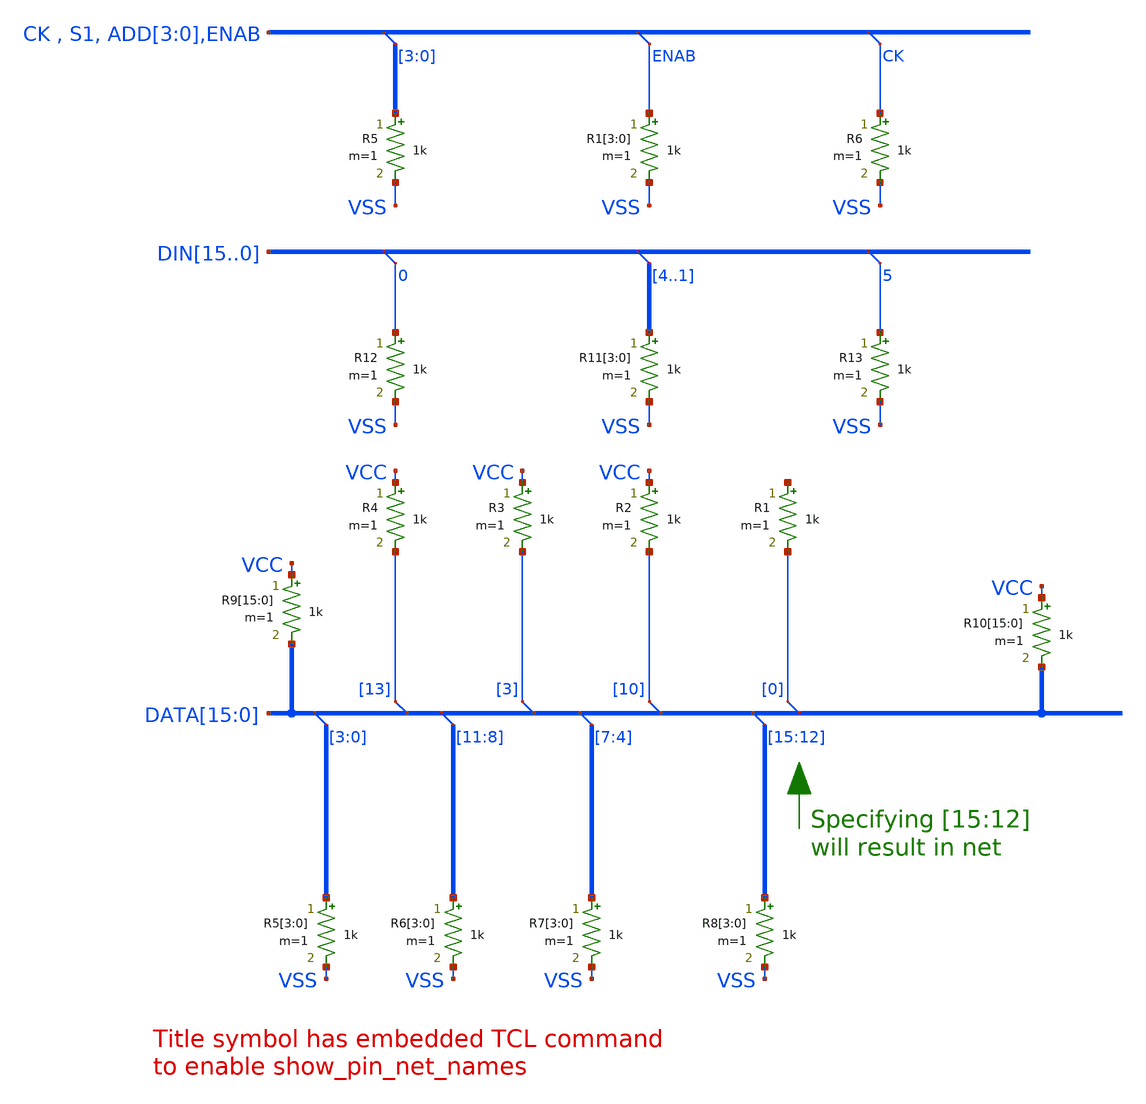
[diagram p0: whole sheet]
** sch_path: xschem_library/examples/test_bus_tap.sch
**.subckt test_bus_tap
* tap: DATA[15:0] --> DATA[3]
* tap: DATA[15:0] --> DATA[13]
* tap: DATA[15:0] --> DATA[7:4]
* tap: DATA[15:0] --> DATA[11:8]
* tap: DATA[15:0] --> DATA[3:0]
* tap: DATA[15:0] --> DATA[10]
* tap: DATA[15:0] --> DATA[0]
R1 net1 DATA[0] 1k m=1
R2 VCC DATA[10] 1k m=1
R3 VCC DATA[3] 1k m=1
R4 VCC DATA[13] 1k m=1
R5[3] DATA[3] VSS 1k m=1
R5[2] DATA[2] VSS 1k m=1
R5[1] DATA[1] VSS 1k m=1
R5[0] DATA[0] VSS 1k m=1
R6[3] DATA[11] VSS 1k m=1
R6[2] DATA[10] VSS 1k m=1
R6[1] DATA[9] VSS 1k m=1
R6[0] DATA[8] VSS 1k m=1
R7[3] DATA[7] VSS 1k m=1
R7[2] DATA[6] VSS 1k m=1
R7[1] DATA[5] VSS 1k m=1
R7[0] DATA[4] VSS 1k m=1
R8[3] DATA[15] VSS 1k m=1
R8[2] DATA[14] VSS 1k m=1
R8[1] DATA[13] VSS 1k m=1
R8[0] DATA[12] VSS 1k m=1
* tap: DATA[15:0] --> DATA[15:12]
R9[15] VCC DATA[15] 1k m=1
R9[14] VCC DATA[14] 1k m=1
R9[13] VCC DATA[13] 1k m=1
R9[12] VCC DATA[12] 1k m=1
R9[11] VCC DATA[11] 1k m=1
R9[10] VCC DATA[10] 1k m=1
R9[9] VCC DATA[9] 1k m=1
R9[8] VCC DATA[8] 1k m=1
R9[7] VCC DATA[7] 1k m=1
R9[6] VCC DATA[6] 1k m=1
R9[5] VCC DATA[5] 1k m=1
R9[4] VCC DATA[4] 1k m=1
R9[3] VCC DATA[3] 1k m=1
R9[2] VCC DATA[2] 1k m=1
R9[1] VCC DATA[1] 1k m=1
R9[0] VCC DATA[0] 1k m=1
R10[15] VCC DATA[15] 1k m=1
R10[14] VCC DATA[14] 1k m=1
R10[13] VCC DATA[13] 1k m=1
R10[12] VCC DATA[12] 1k m=1
R10[11] VCC DATA[11] 1k m=1
R10[10] VCC DATA[10] 1k m=1
R10[9] VCC DATA[9] 1k m=1
R10[8] VCC DATA[8] 1k m=1
R10[7] VCC DATA[7] 1k m=1
R10[6] VCC DATA[6] 1k m=1
R10[5] VCC DATA[5] 1k m=1
R10[4] VCC DATA[4] 1k m=1
R10[3] VCC DATA[3] 1k m=1
R10[2] VCC DATA[2] 1k m=1
R10[1] VCC DATA[1] 1k m=1
R10[0] VCC DATA[0] 1k m=1
* tap: DIN[15..0] --> DIN0
* tap: DIN[15..0] --> DIN[4..1]
R11[3] DIN4 VSS 1k m=1
R11[2] DIN3 VSS 1k m=1
R11[1] DIN2 VSS 1k m=1
R11[0] DIN1 VSS 1k m=1
R12 DIN0 VSS 1k m=1
* tap: DIN[15..0] --> DIN5
R13 DIN5 VSS 1k m=1
* tap: CK , S1, ADD[3:0],ENAB --> ADD[3:0]
* tap: CK , S1, ADD[3:0],ENAB --> ENAB
R1[3] ENAB VSS 1k m=1
R1[2] ENAB VSS 1k m=1
R1[1] ENAB VSS 1k m=1
R1[0] ENAB VSS 1k m=1
R5 ADD[3] VSS 1k m=1
* tap: CK , S1, ADD[3:0],ENAB --> CK
R6 CK VSS 1k m=1
**.ends
.end
